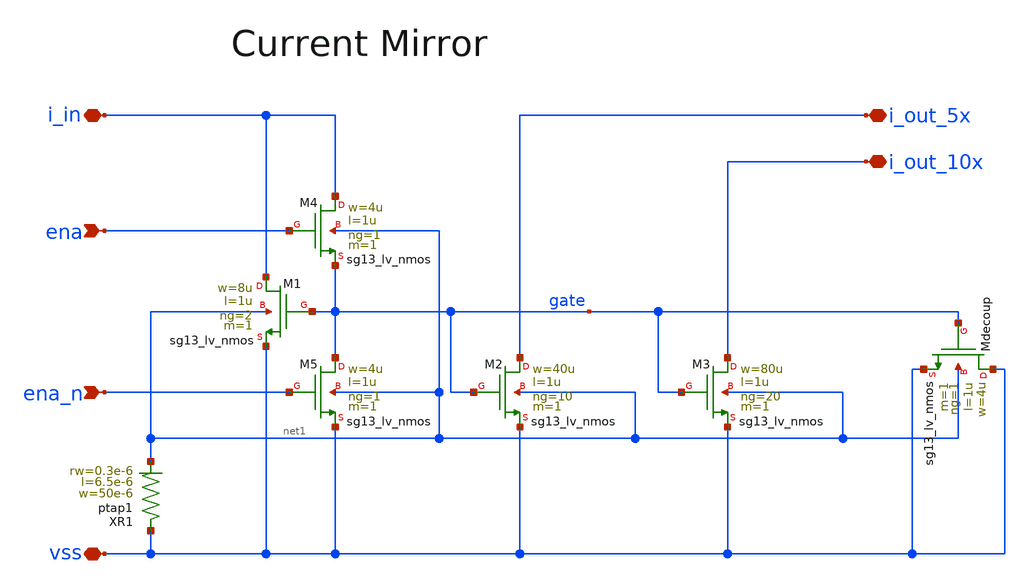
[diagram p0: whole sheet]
** sch_path: dcic_script_current_mirror.sch
* (c) 2026 Julian Schwarz, Apache-2.0 license
**.subckt dcic_script_current_mirror vss i_out_5x i_out_10x i_in ena ena_n
*.iopin vss
*.iopin i_out_5x
*.iopin i_out_10x
*.iopin i_in
*.ipin ena
*.ipin ena_n
XM1 i_in gate vss net1 sg13_lv_nmos w=8u l=1u ng=2 m=1 mm_ok=1
XM2 i_out_5x gate vss net1 sg13_lv_nmos w=40u l=1u ng=10 m=1 mm_ok=1
XM3 i_out_10x gate vss net1 sg13_lv_nmos w=80u l=1u ng=20 m=1 mm_ok=1
XM4 i_in ena gate net1 sg13_lv_nmos w=4u l=1u ng=1 m=1 mm_ok=1
XM5 gate ena_n vss net1 sg13_lv_nmos w=4u l=1u ng=1 m=1 mm_ok=1
XMdecoup vss gate vss net1 sg13_lv_nmos w=4u l=1u ng=1 m=1 mm_ok=1
XR1 vss net1 ptap1 R=2.039 w=50e-6 l=6.5e-6 rw=0.3e-6
**.ends
.end
